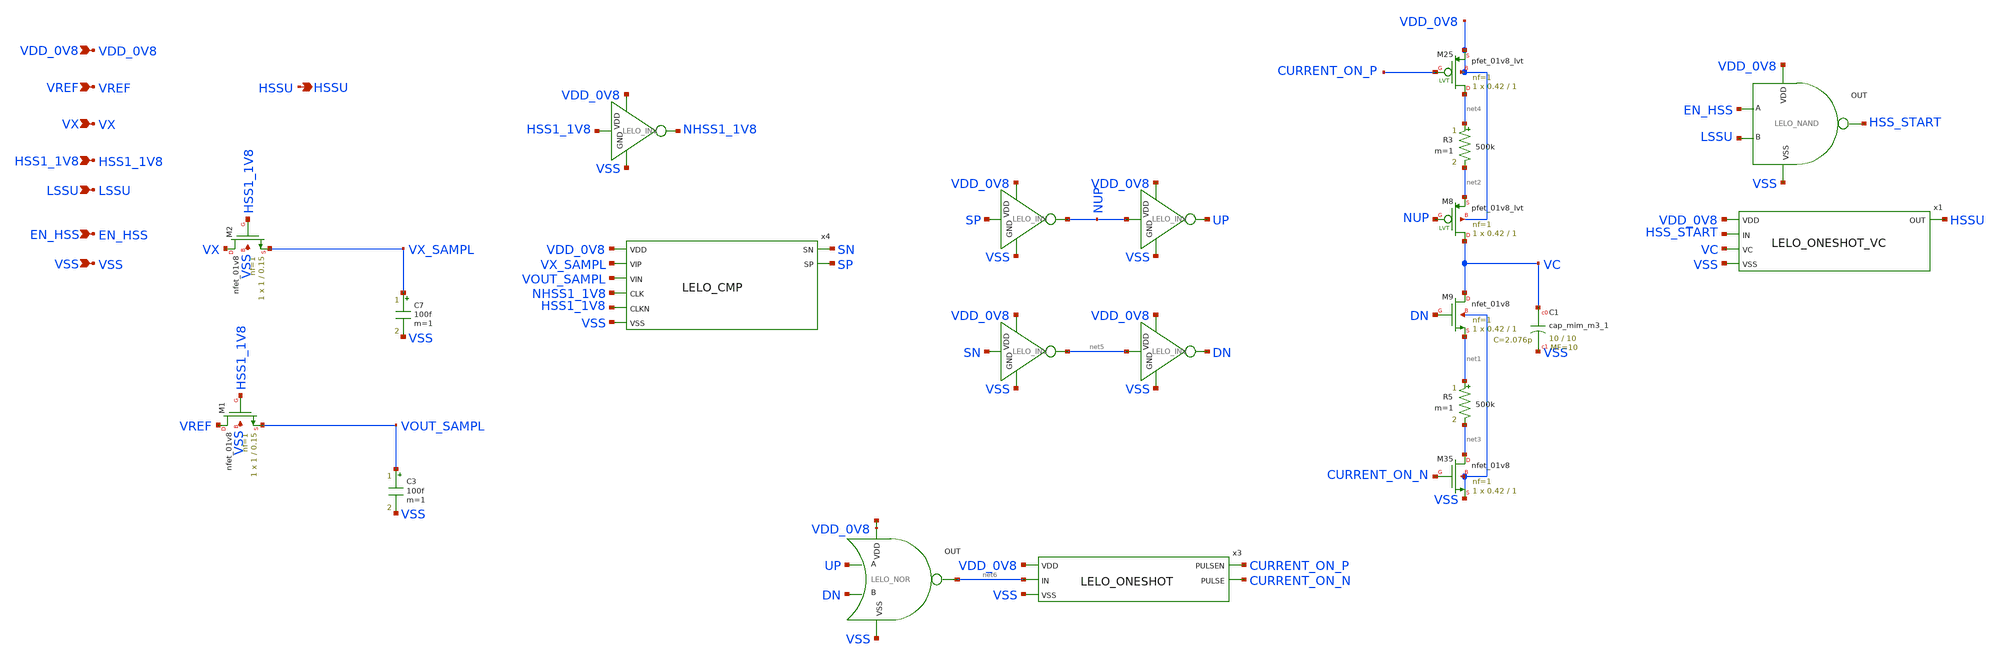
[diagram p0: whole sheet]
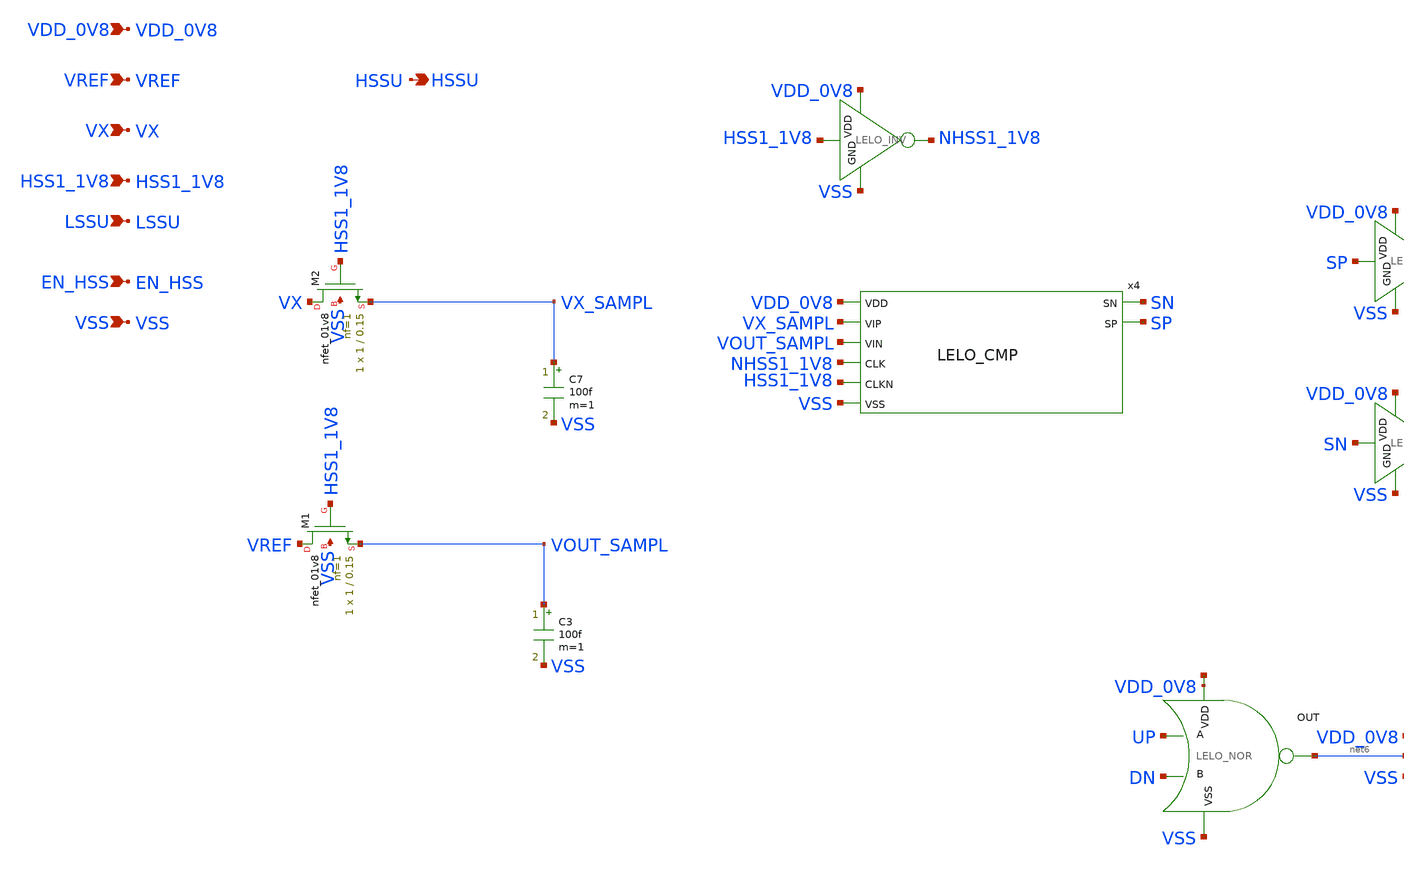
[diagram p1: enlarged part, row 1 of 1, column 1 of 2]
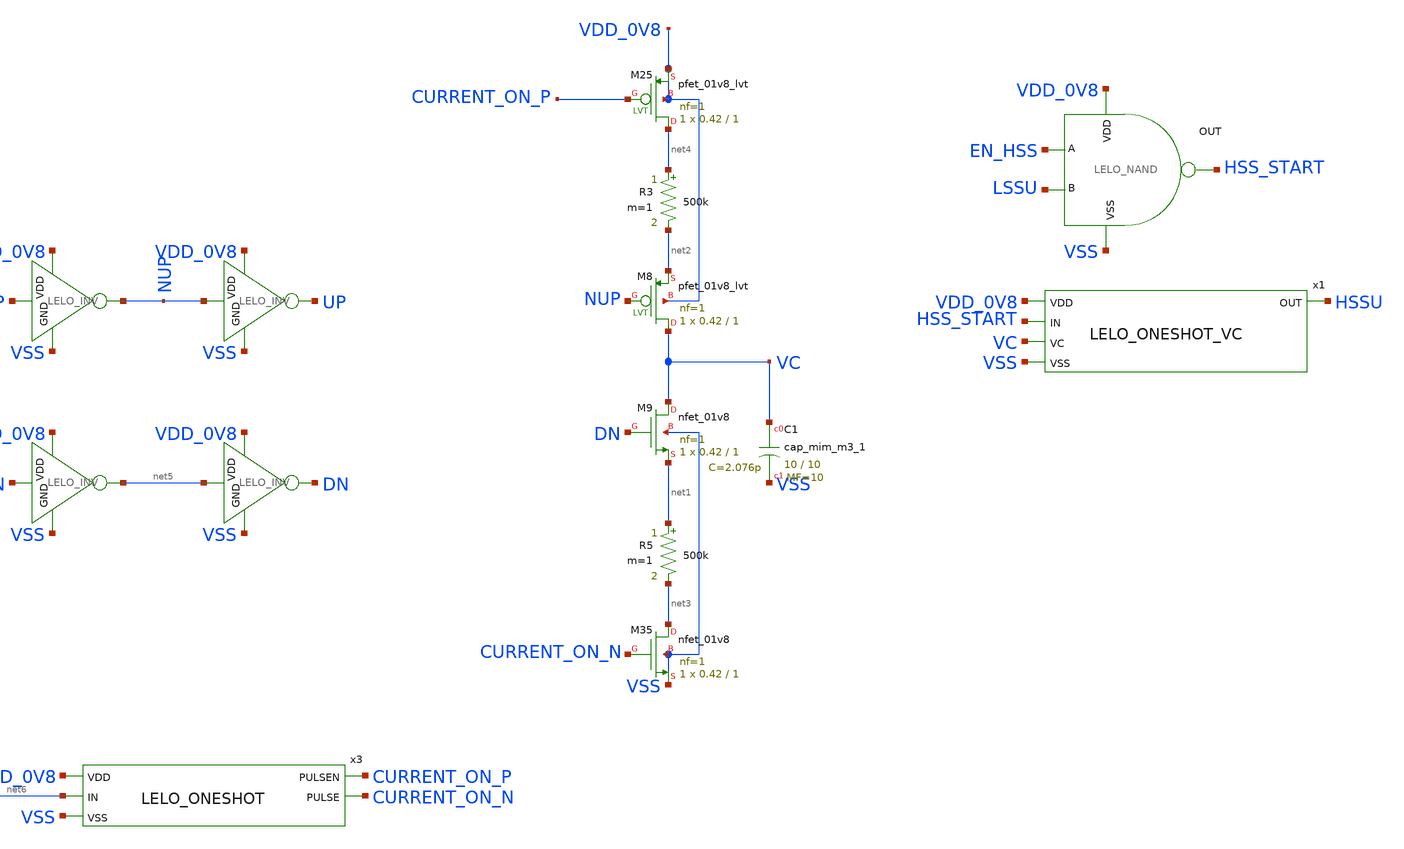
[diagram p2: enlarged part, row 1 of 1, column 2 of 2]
** sch_path: design/LELO_SVOD_SKY130A/LELO_SVOD_HSSCNTRL.sch
**.subckt LELO_SVOD_HSSCNTRL VREF HSSU VX LSSU VSS EN_HSS VDD_0V8 HSS1_1V8
*.ipin VREF
*.opin HSSU
*.ipin VX
*.ipin LSSU
*.ipin VSS
*.ipin EN_HSS
*.ipin VDD_0V8
*.ipin HSS1_1V8
C7 VX_SAMPL VSS 100f m=1
C3 VOUT_SAMPL VSS 100f m=1
x4 SN SP VDD_0V8 VX_SAMPL VOUT_SAMPL NHSS1_1V8 HSS1_1V8 VSS LELO_CMP
XM9 VC DN net1 VSS sky130_fd_pr__nfet_01v8 L=1 W=0.42 nf=1 ad='int((1 + 1)/2) * 0.42 / 1 * 0.29' as='int((1 + 2)/2) * 0.42 / 1 * 0.29'
+ pd='2*int((1 + 1)/2) * (0.42 / 1 + 0.29)' ps='2*int((1 + 2)/2) * (0.42 / 1 + 0.29)' nrd='0.29 / 0.42 '
+ nrs='0.29 / 0.42 ' sa=0 sb=0 sd=0 mult=1 m=1
x10 VDD_0V8 SP NUP VSS LELO_INV
R5 net1 net3 500k m=1
XM35 net3 CURRENT_ON_N VSS VSS sky130_fd_pr__nfet_01v8 L=1 W=0.42 nf=1 ad='int((1 + 1)/2) * 0.42 / 1 * 0.29'
+ as='int((1 + 2)/2) * 0.42 / 1 * 0.29' pd='2*int((1 + 1)/2) * (0.42 / 1 + 0.29)' ps='2*int((1 + 2)/2) * (0.42 / 1 + 0.29)'
+ nrd='0.29 / 0.42 ' nrs='0.29 / 0.42 ' sa=0 sb=0 sd=0 mult=1 m=1
x11 VDD_0V8 SN net5 VSS LELO_INV
x14 VDD_0V8 net5 DN VSS LELO_INV
x17 VDD_0V8 NUP UP VSS LELO_INV
x2 net7 net6 UP DN VSS LELO_NOR
x3 VDD_0V8 net6 VSS CURRENT_ON_P CURRENT_ON_N LELO_ONESHOT
R3 net4 net2 500k m=1
XM8 VC NUP net2 VDD_0V8 sky130_fd_pr__pfet_01v8_lvt L=1 W=0.42 nf=1 ad='int((1 + 1)/2) * 0.42 / 1 * 0.29'
+ as='int((1 + 2)/2) * 0.42 / 1 * 0.29' pd='2*int((1 + 1)/2) * (0.42 / 1 + 0.29)' ps='2*int((1 + 2)/2) * (0.42 / 1 + 0.29)'
+ nrd='0.29 / 0.42 ' nrs='0.29 / 0.42 ' sa=0 sb=0 sd=0 mult=1 m=1
XM25 net4 CURRENT_ON_P VDD_0V8 VDD_0V8 sky130_fd_pr__pfet_01v8_lvt L=1 W=0.42 nf=1 ad='int((1 + 1)/2) * 0.42 / 1 * 0.29'
+ as='int((1 + 2)/2) * 0.42 / 1 * 0.29' pd='2*int((1 + 1)/2) * (0.42 / 1 + 0.29)' ps='2*int((1 + 2)/2) * (0.42 / 1 + 0.29)'
+ nrd='0.29 / 0.42 ' nrs='0.29 / 0.42 ' sa=0 sb=0 sd=0 mult=1 m=1
x1 VDD_0V8 HSS_START VC HSSU VSS LELO_ONESHOT_VC
XM1 VREF HSS1_1V8 VOUT_SAMPL VSS sky130_fd_pr__nfet_01v8 L=0.15 W=1 nf=1 ad='int((1 + 1)/2) * 1 / 1 * 0.29'
+ as='int((1 + 2)/2) * 1 / 1 * 0.29' pd='2*int((1 + 1)/2) * (1 / 1 + 0.29)' ps='2*int((1 + 2)/2) * (1 / 1 + 0.29)'
+ nrd='0.29 / 1 ' nrs='0.29 / 1 ' sa=0 sb=0 sd=0 mult=1 m=1
XM2 VX HSS1_1V8 VX_SAMPL VSS sky130_fd_pr__nfet_01v8 L=0.15 W=1 nf=1 ad='int((1 + 1)/2) * 1 / 1 * 0.29'
+ as='int((1 + 2)/2) * 1 / 1 * 0.29' pd='2*int((1 + 1)/2) * (1 / 1 + 0.29)' ps='2*int((1 + 2)/2) * (1 / 1 + 0.29)'
+ nrd='0.29 / 1 ' nrs='0.29 / 1 ' sa=0 sb=0 sd=0 mult=1 m=1
x6 VDD_0V8 HSS_START EN_HSS LSSU VSS LELO_NAND
x5 VDD_0V8 HSS1_1V8 NHSS1_1V8 VSS LELO_INV
XC1 VC VSS sky130_fd_pr__cap_mim_m3_1 W=10 L=10 MF=10 m=10
**.ends
.end
